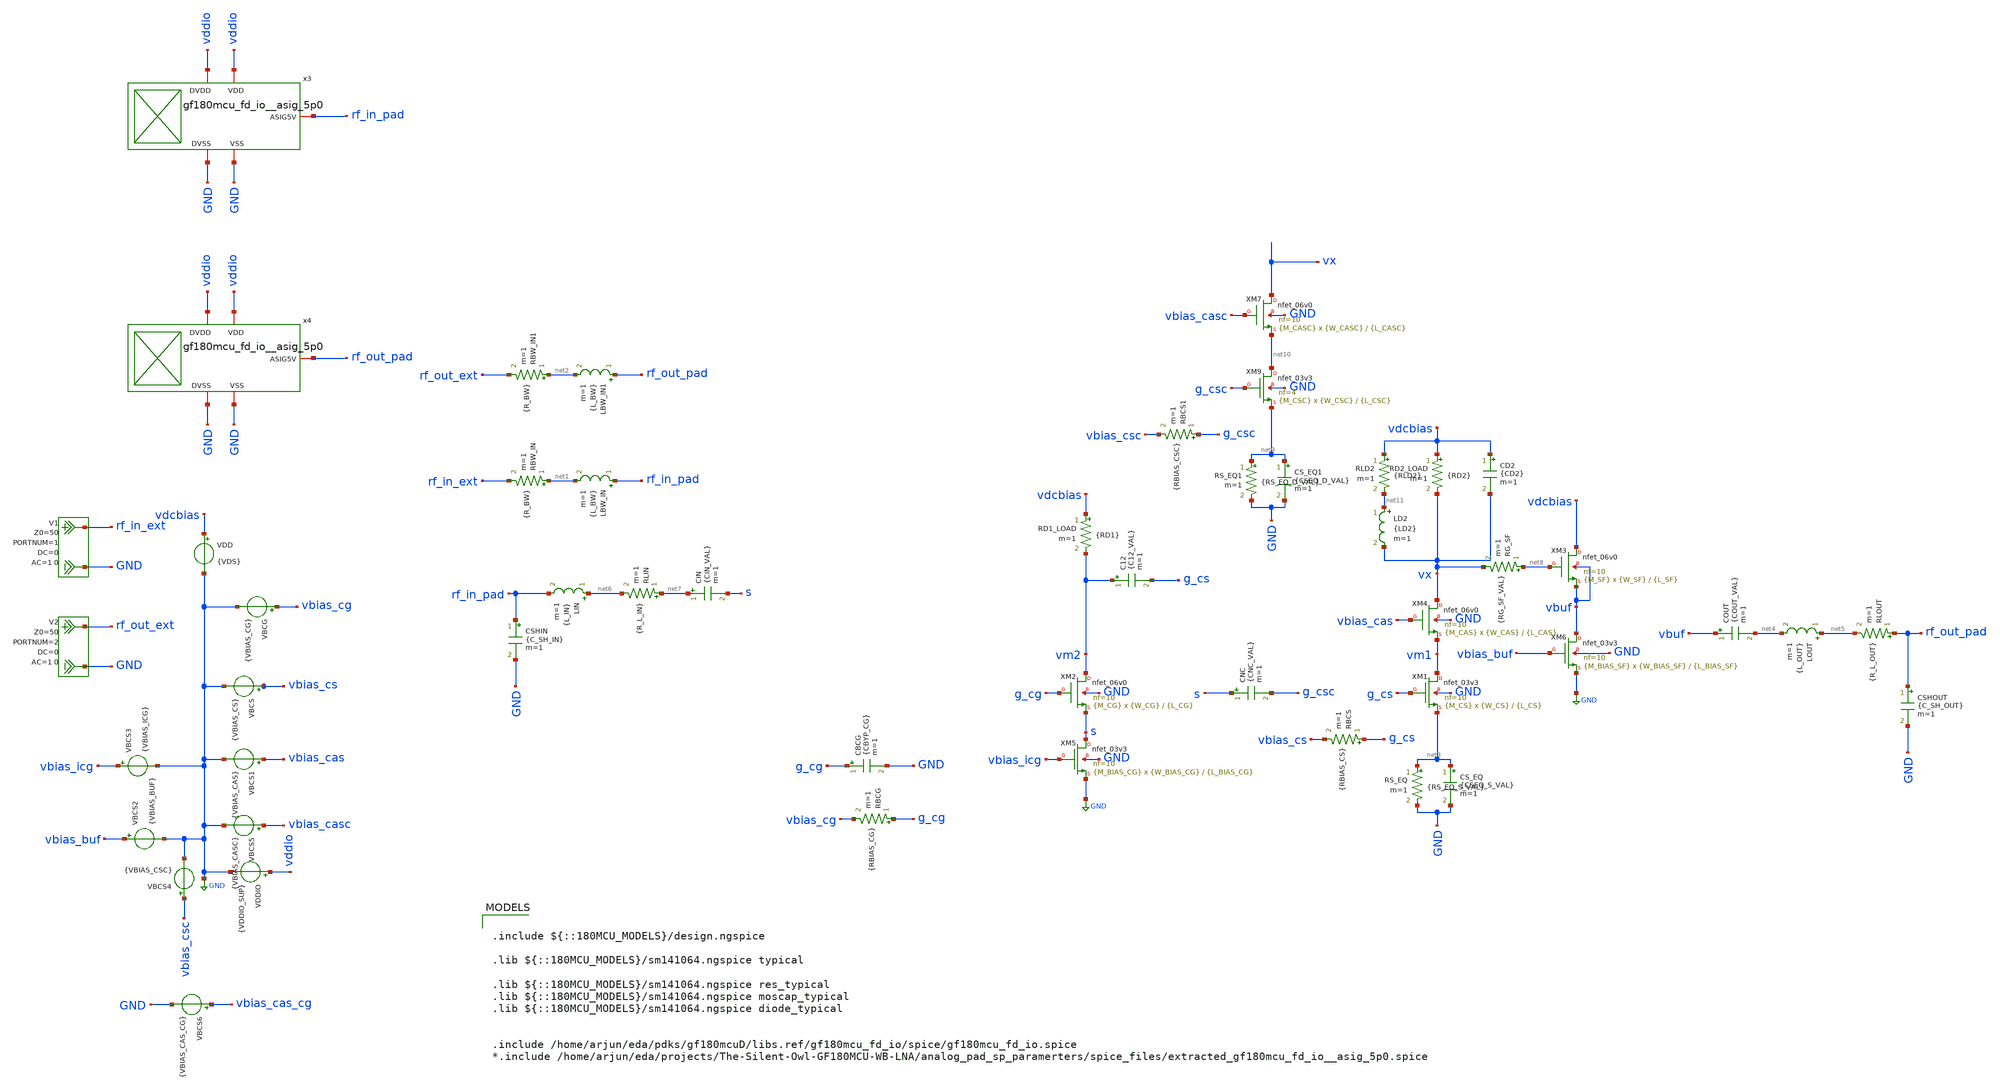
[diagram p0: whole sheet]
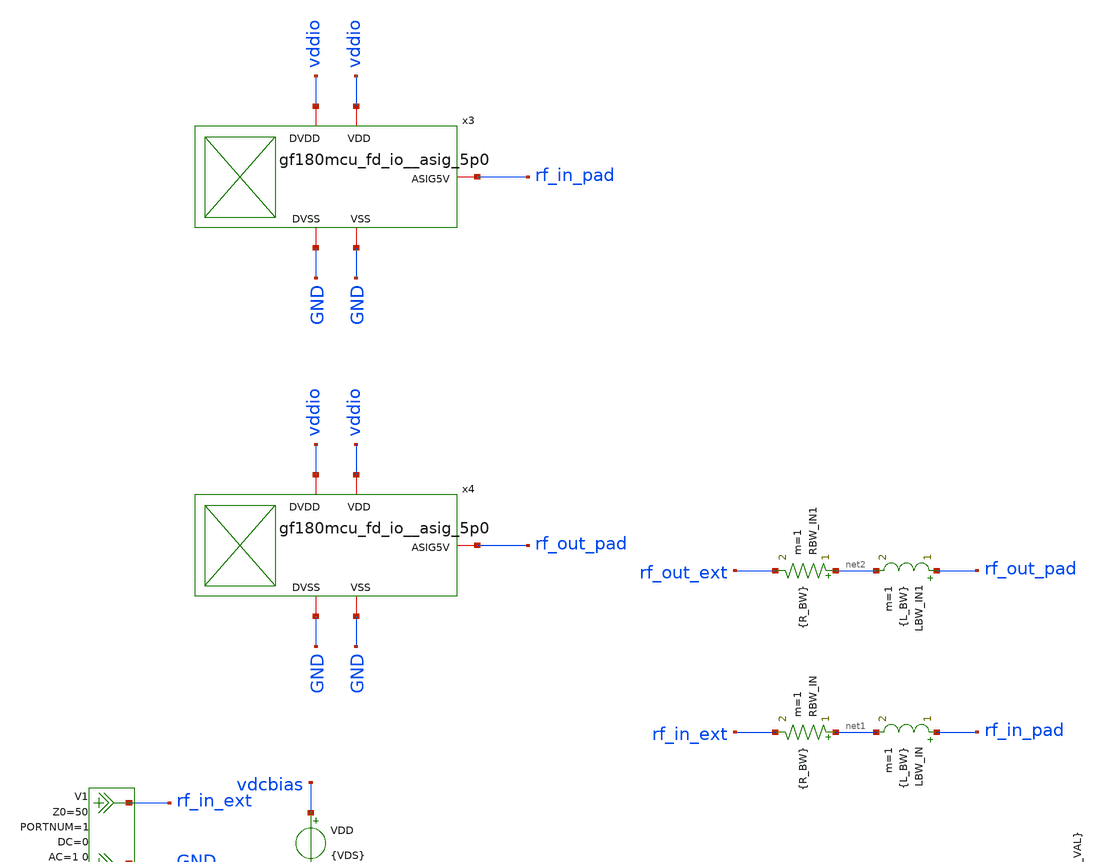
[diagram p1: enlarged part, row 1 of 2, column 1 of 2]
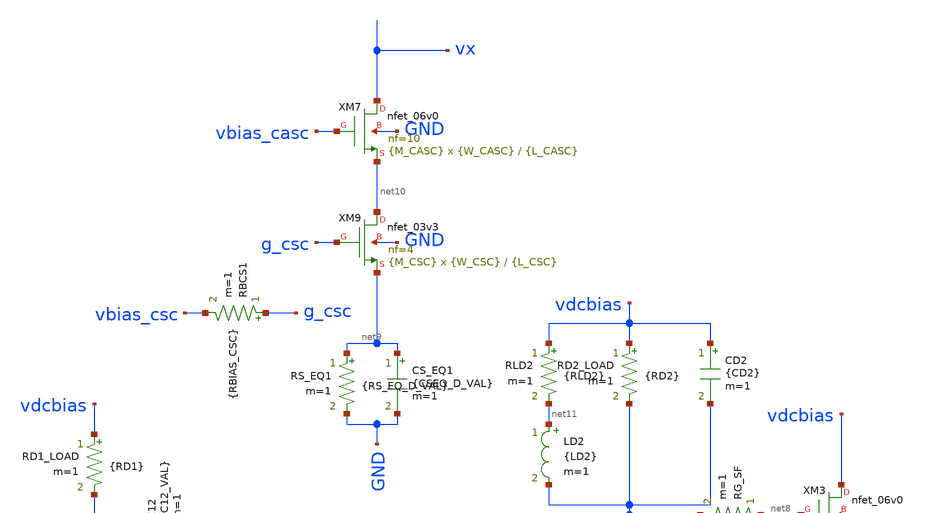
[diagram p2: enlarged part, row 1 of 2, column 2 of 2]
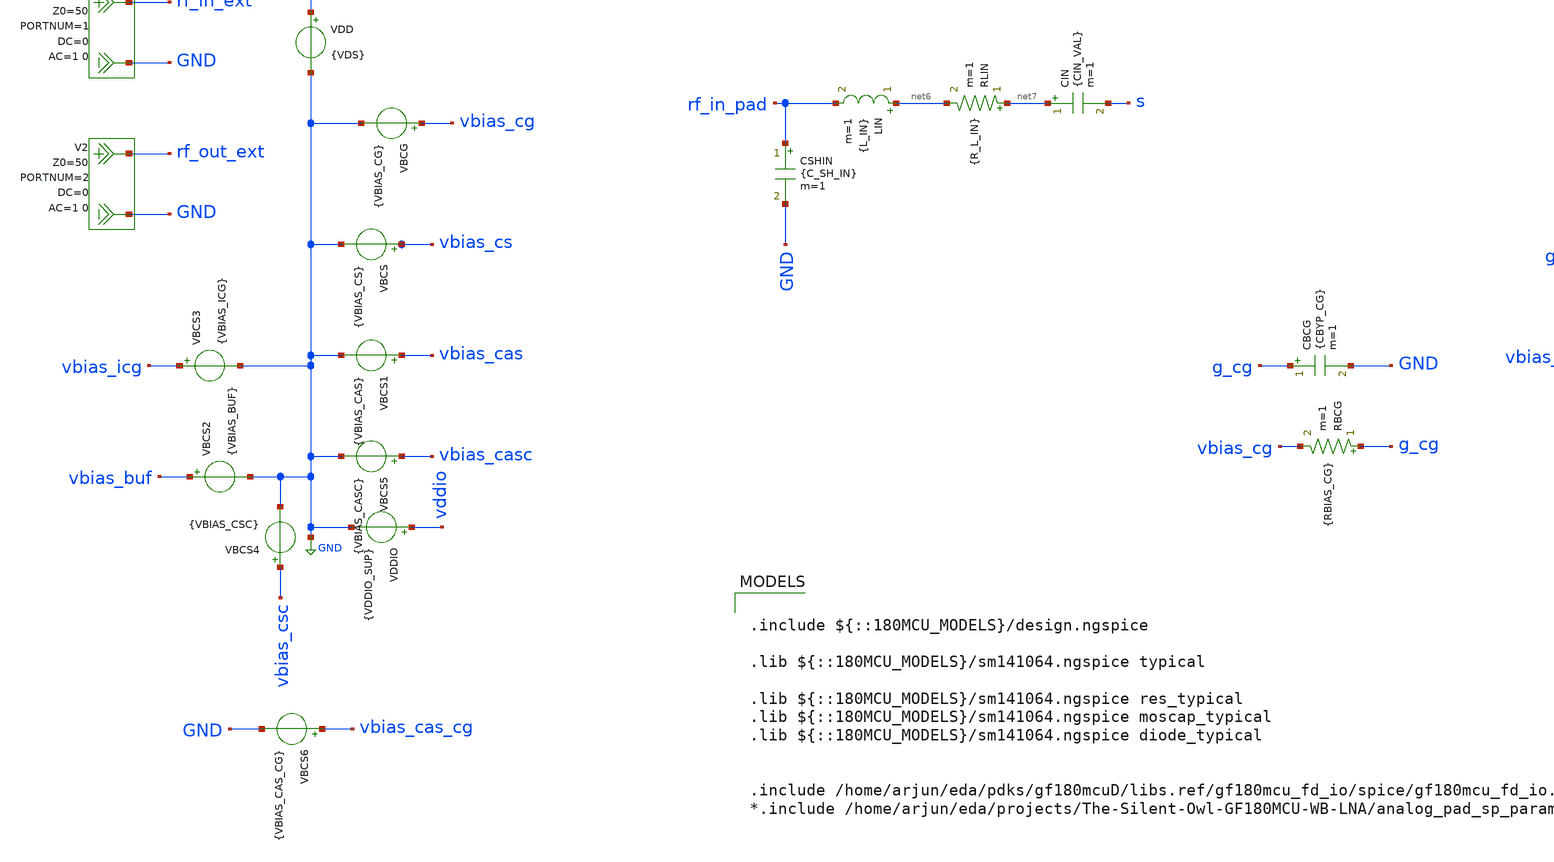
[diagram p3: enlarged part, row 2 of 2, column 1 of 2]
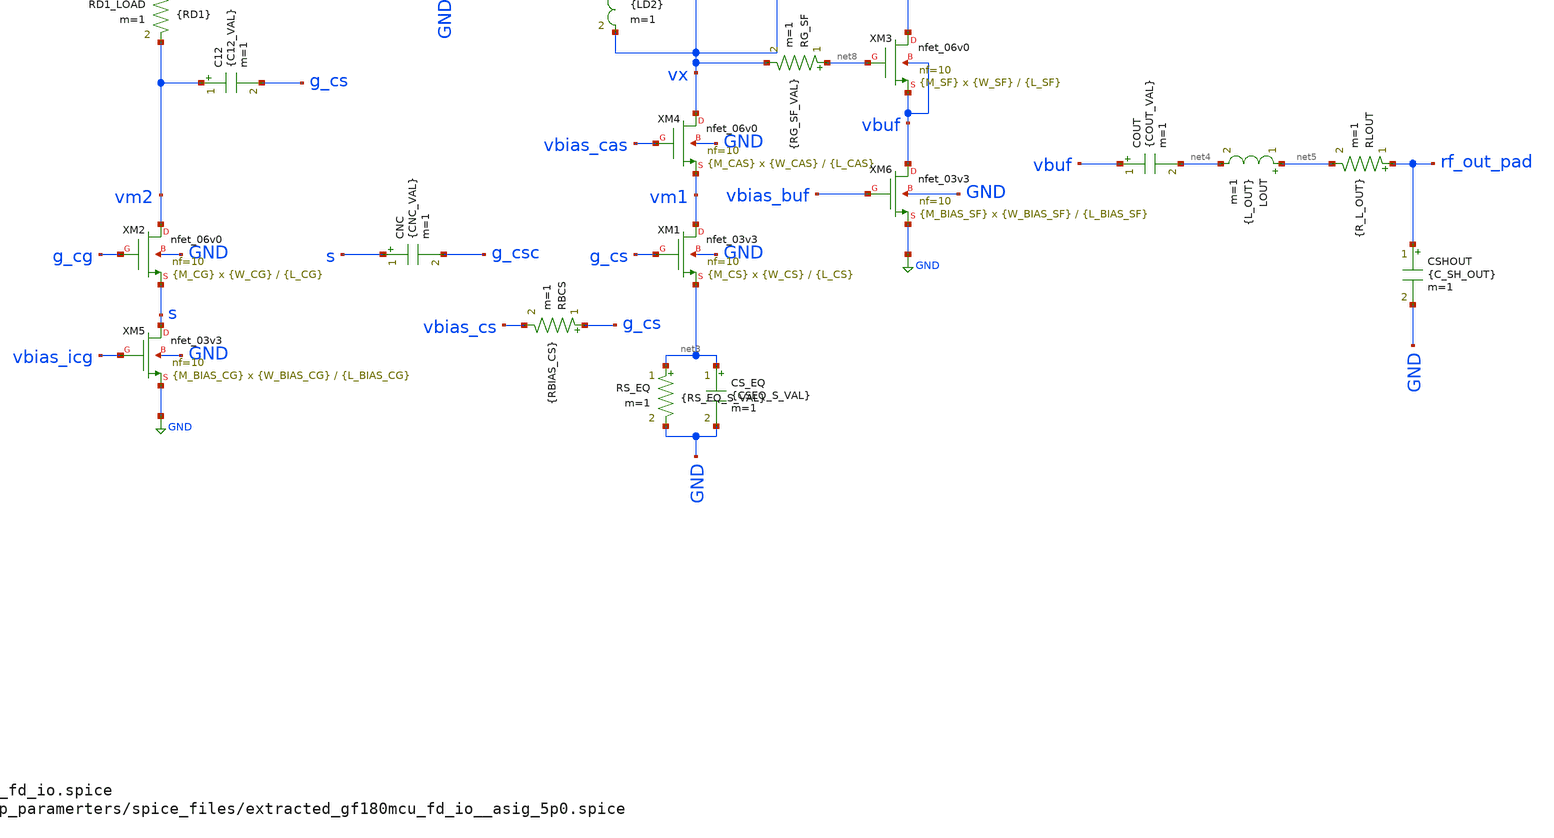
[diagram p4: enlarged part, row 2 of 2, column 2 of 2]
** sch_path: NFmin_Simulation/simulations/lna_core_06V_cgcs_sweep-1.sch
**.subckt lna_core_06V_cgcs_sweep-1
VBCG vbias_cg GND {VBIAS_CG}
VDD vdcbias GND {VDS}
C12 vm2 g_cs {C12_VAL} m=1
CIN net7 s {CIN_VAL} m=1
V1 rf_in_ext GND DC 0 AC 1 0 portnum 1 z0 50
V2 rf_out_ext GND DC 0 AC 1 0 portnum 2 z0 50
XM2 vm2 g_cg s GND nfet_06v0 L={L_CG} W={W_CG} nf=10 ad='int((nf+1)/2) * W/nf * 0.18u' as='int((nf+2)/2) * W/nf * 0.18u'
+ pd='2*int((nf+1)/2) * (W/nf + 0.18u)' ps='2*int((nf+2)/2) * (W/nf + 0.18u)' nrd='0.18u / W' nrs='0.18u / W'
+ sa=0 sb=0 sd=0 m={M_CG}
RBCG g_cg vbias_cg {RBIAS_CG} m=1
CBCG g_cg GND {CBYP_CG} m=1
LBW_IN rf_in_pad net1 {L_BW} m=1
RBW_IN net1 rf_in_ext {R_BW} m=1
VDDIO vddio GND {VDDIO_SUP}
LBW_IN1 rf_out_pad net2 {L_BW} m=1
RBW_IN1 net2 rf_out_ext {R_BW} m=1
VBCS vbias_cs GND {VBIAS_CS}
RD1_LOAD vdcbias vm2 {RD1} m=1
RBCS g_cs vbias_cs {RBIAS_CS} m=1
RD2_LOAD vdcbias vx {RD2} m=1
XM3 vdcbias net8 vbuf vbuf nfet_06v0 L={L_SF} W={W_SF} nf=10 ad='int((nf+1)/2) * W/nf * 0.18u' as='int((nf+2)/2) * W/nf * 0.18u'
+ pd='2*int((nf+1)/2) * (W/nf + 0.18u)' ps='2*int((nf+2)/2) * (W/nf + 0.18u)' nrd='0.18u / W' nrs='0.18u / W'
+ sa=0 sb=0 sd=0 m={M_SF}
COUT vbuf net4 {COUT_VAL} m=1
LOUT net5 net4 {L_OUT} m=1
RLOUT rf_out_pad net5 {R_L_OUT} m=1
CSHOUT rf_out_pad GND {C_SH_OUT} m=1
CSHIN rf_in_pad GND {C_SH_IN} m=1
LIN net6 rf_in_pad {L_IN} m=1
RLIN net7 net6 {R_L_IN} m=1
XM4 vx vbias_cas vm1 GND nfet_06v0 L={L_CAS} W={W_CAS} nf=10 ad='int((nf+1)/2) * W/nf * 0.18u' as='int((nf+2)/2) * W/nf * 0.18u'
+ pd='2*int((nf+1)/2) * (W/nf + 0.18u)' ps='2*int((nf+2)/2) * (W/nf + 0.18u)' nrd='0.18u / W' nrs='0.18u / W'
+ sa=0 sb=0 sd=0 m={M_CAS}
VBCS1 vbias_cas GND {VBIAS_CAS}
VBCS2 vbias_buf GND {VBIAS_BUF}
VBCS3 vbias_icg GND {VBIAS_ICG}
XM5 s vbias_icg GND GND nfet_03v3 L={L_BIAS_CG} W={W_BIAS_CG} nf=10 ad='int((nf+1)/2) * W/nf * 0.18u'
+ as='int((nf+2)/2) * W/nf * 0.18u' pd='2*int((nf+1)/2) * (W/nf + 0.18u)' ps='2*int((nf+2)/2) * (W/nf + 0.18u)'
+ nrd='0.18u / W' nrs='0.18u / W' sa=0 sb=0 sd=0 m={M_BIAS_CG}
XM6 vbuf vbias_buf GND GND nfet_03v3 L={L_BIAS_SF} W={W_BIAS_SF} nf=10 ad='int((nf+1)/2) * W/nf * 0.18u'
+ as='int((nf+2)/2) * W/nf * 0.18u' pd='2*int((nf+1)/2) * (W/nf + 0.18u)' ps='2*int((nf+2)/2) * (W/nf + 0.18u)'
+ nrd='0.18u / W' nrs='0.18u / W' sa=0 sb=0 sd=0 m={M_BIAS_SF}
RS_EQ net3 GND {RS_EQ_S_VAL} m=1
CS_EQ net3 GND {CSEQ_S_VAL} m=1
XM1 vm1 g_cs net3 GND nfet_03v3 L={L_CS} W={W_CS} nf=10 ad='int((nf+1)/2) * W/nf * 0.18u' as='int((nf+2)/2) * W/nf * 0.18u'
+ pd='2*int((nf+1)/2) * (W/nf + 0.18u)' ps='2*int((nf+2)/2) * (W/nf + 0.18u)' nrd='0.18u / W' nrs='0.18u / W'
+ sa=0 sb=0 sd=0 m={M_CS}
RG_SF net8 vx {RG_SF_VAL} m=1
x3 rf_in_pad vddio GND vddio GND gf180mcu_fd_io__asig_5p0
x4 rf_out_pad vddio GND vddio GND gf180mcu_fd_io__asig_5p0
RBCS1 g_csc vbias_csc {RBIAS_CSC} m=1
XM7 vx vbias_casc net10 GND nfet_06v0 L={L_CASC} W={W_CASC} nf=10 ad='int((nf+1)/2) * W/nf * 0.18u' as='int((nf+2)/2) * W/nf * 0.18u'
+ pd='2*int((nf+1)/2) * (W/nf + 0.18u)' ps='2*int((nf+2)/2) * (W/nf + 0.18u)' nrd='0.18u / W' nrs='0.18u / W'
+ sa=0 sb=0 sd=0 m={M_CASC}
RS_EQ1 net9 GND {RS_EQ_D_VAL} m=1
CS_EQ1 net9 GND {CSEQ_D_VAL} m=1
XM9 net10 g_csc net9 GND nfet_03v3 L={L_CSC} W={W_CSC} nf=4 ad='int((nf+1)/2) * W/nf * 0.18u' as='int((nf+2)/2) * W/nf * 0.18u'
+ pd='2*int((nf+1)/2) * (W/nf + 0.18u)' ps='2*int((nf+2)/2) * (W/nf + 0.18u)' nrd='0.18u / W' nrs='0.18u / W'
+ sa=0 sb=0 sd=0 m={M_CSC}
VBCS4 vbias_csc GND {VBIAS_CSC}
VBCS5 vbias_casc GND {VBIAS_CASC}
CNC s g_csc {CNC_VAL} m=1
VBCS6 vbias_cas_cg GND {VBIAS_CAS_CG}
LD2 net11 vx {LD2} m=1
CD2 vdcbias vx {CD2} m=1
RLD2 vdcbias net11 {RLD2} m=1
**** begin user architecture code

.include ${::180MCU_MODELS}/design.ngspice

.lib ${::180MCU_MODELS}/sm141064.ngspice typical

.lib ${::180MCU_MODELS}/sm141064.ngspice res_typical
.lib ${::180MCU_MODELS}/sm141064.ngspice moscap_typical
.lib ${::180MCU_MODELS}/sm141064.ngspice diode_typical


.include /home/arjun/eda/pdks/gf180mcuD/libs.ref/gf180mcu_fd_io/spice/gf180mcu_fd_io.spice
*.include /home/arjun/eda/projects/The-Silent-Owl-GF180MCU-WB-LNA/analog_pad_sp_paramerters/spice_files/extracted_gf180mcu_fd_io__asig_5p0.spice



* =============================================================================
* BEST OPTIMIZED PARAMETER SET
* =============================================================================
.param RLD2=7
* Currently unused unless a corresponding cascode-CG transistor is instantiated
.param VBIAS_CAS_CG=3.30
.param L_CAS_CG=0.60u
.param W_CAS_CG=80u
.param M_CAS_CG=4

* -----------------------------------------------------------------------------
* Supply / package
* -----------------------------------------------------------------------------
.param VDS=5.0
.param VDDIO_SUP=5.0

.param L_BW=2n
.param R_BW=0.2

* -----------------------------------------------------------------------------
* Source equalization networks
* -----------------------------------------------------------------------------

* XM9 cancellation-branch source equalizer
.param RS_EQ_D_VAL=0.25
.param CSEQ_D_VAL=4.7p

* XM1 main-path source equalizer
.param RS_EQ_S_VAL=0.10
.param CSEQ_S_VAL=220f

* Redundant aliases retained for compatibility
.param RS_EQ=0.10
.param CSEQ_VAL=220f

* -----------------------------------------------------------------------------
* Input network
*
* Package inductance       = 2.0 nH
* Intentional inductance   = 3.5 nH
* Total nominal inductance = 5.5 nH, excluding pad/interconnect parasitics
* -----------------------------------------------------------------------------
.param L_IN=3.5n
.param R_L_IN=2.26

.param CIN_VAL=8.2p
.param C_SH_IN=330f

* -----------------------------------------------------------------------------
* XM2 common-gate input stage
* -----------------------------------------------------------------------------
.param VBIAS_CG=2.10

.param W_CG=40u
.param M_CG=10
.param L_CG=0.60u

.param RD1=950

.param RBIAS_CG=50k
.param CBYP_CG=20p

* -----------------------------------------------------------------------------
* XM1 common-source / XM4 cascode main stage
* -----------------------------------------------------------------------------
.param C12_VAL=8.2p

.param VBIAS_CS=1.25

.param W_CS=20u
.param M_CS=8
.param L_CS=0.28u

.param RBIAS_CS=50k

.param VBIAS_CAS=3.60

.param W_CAS=35u
.param M_CAS=4
.param L_CAS=0.60u

.param RD2=1.2k

* -----------------------------------------------------------------------------
* XM3 body-tied source follower
* -----------------------------------------------------------------------------
.param W_SF=25u
.param M_SF=8
.param L_SF=0.60u

.param RG_SF_VAL=0.10

* -----------------------------------------------------------------------------
* Output network
*
* Package inductance       = 2.0 nH
* Intentional inductance   = 1.2 nH
* Total nominal inductance = 3.2 nH, excluding pad/interconnect parasitics
* -----------------------------------------------------------------------------
.param COUT_VAL=4.7p

.param L_OUT=1.2n
.param R_L_OUT=1.5

.param C_SH_OUT=470f

* -----------------------------------------------------------------------------
* XM5 common-gate current sink
* -----------------------------------------------------------------------------
.param VBIAS_ICG=1.80

.param L_BIAS_CG=0.50u
.param W_BIAS_CG=15u
.param M_BIAS_CG=1

* -----------------------------------------------------------------------------
* XM6 source-follower current sink
* -----------------------------------------------------------------------------
.param VBIAS_BUF=2.50

.param L_BIAS_SF=0.50u
.param W_BIAS_SF=25u
.param M_BIAS_SF=5

* -----------------------------------------------------------------------------
* XM9 source-sensing common-source cancellation branch
* -----------------------------------------------------------------------------
.param RBIAS_CSC=50k

.param VBIAS_CSC=0.90

.param L_CSC=0.28u
.param W_CSC=40u
.param M_CSC=6
.param NF_CSC=4

* -----------------------------------------------------------------------------
* XM7 cancellation-branch cascode
* -----------------------------------------------------------------------------
.param VBIAS_CASC=3.40

.param L_CASC=0.60u
.param W_CASC=35u
.param M_CASC=1

* -----------------------------------------------------------------------------
* Noise-cancellation coupling capacitor
* -----------------------------------------------------------------------------
.param CNC_VAL=8.2p

* -----------------------------------------------------------------------------
* Drain shunt-peaking network
* -----------------------------------------------------------------------------
.param LD2=4.7n
.param CD2=680f
.param R_LD2=7





.control

set noaskquit
set wr_singlescale
set wr_vecnames
set numdgt=10

let target_gain_bw=10.0

echo ============================================================ > lna_core_06V_cgcs_report.txt
echo GF180MCU_LNA_CORE_06V_CGCS_DETAILED_REPORT >> lna_core_06V_cgcs_report.txt
echo TARGET_FREQUENCY_HZ 2.400e9 >> lna_core_06V_cgcs_report.txt
echo TARGET_BAND_HZ 2.300e9 2.500e9 >> lna_core_06V_cgcs_report.txt
echo GAIN_BANDWIDTH_THRESHOLD_DB 10.0 >> lna_core_06V_cgcs_report.txt
echo PORT_REFERENCE_OHM 50 >> lna_core_06V_cgcs_report.txt
echo ============================================================ >> lna_core_06V_cgcs_report.txt

* =============================================================================
* DC OPERATING POINT
* =============================================================================

op

let pdcop=1e3*(abs(i(VDD))*v(vdcbias)+abs(i(VDDIO))*v(vddio))
let icoreop=abs(i(VDD))
let iioop=abs(i(VDDIO))

let vsop=v(s)
let vdop=v(vm2)
let vnet3op=v(net3)
let vnet8op=v(net8)
let vbufop=v(vbuf)
let vgcsop=v(g_cs)
let vgcgop=v(g_cg)

let id1op=abs(@m.xm1.m0[id])
let gm1op=@m.xm1.m0[gm]
let gmb1op=@m.xm1.m0[gmbs]
let gds1op=@m.xm1.m0[gds]
let vgs1op=@m.xm1.m0[vgs]
let vds1op=@m.xm1.m0[vds]
let vbs1op=@m.xm1.m0[vbs]
let vth1op=@m.xm1.m0[vth]
let vov1op=vgs1op-vth1op
let vdsat1op=abs(@m.xm1.m0[vdsat])
let sat1op=vds1op-vdsat1op
let gmid1op=gm1op/(id1op+1e-30)
let ro1op=1/(gds1op+1e-30)

let id2op=abs(@m.xm2.m0[id])
let gm2op=@m.xm2.m0[gm]
let gmb2op=@m.xm2.m0[gmbs]
let gds2op=@m.xm2.m0[gds]
let vgs2op=@m.xm2.m0[vgs]
let vds2op=@m.xm2.m0[vds]
let vbs2op=@m.xm2.m0[vbs]
let vth2op=@m.xm2.m0[vth]
let vov2op=vgs2op-vth2op
let vdsat2op=abs(@m.xm2.m0[vdsat])
let sat2op=vds2op-vdsat2op
let gmid2op=gm2op/(id2op+1e-30)
let ro2op=1/(gds2op+1e-30)

let id3op=abs(@m.xm3.m0[id])
let gm3op=@m.xm3.m0[gm]
let gmb3op=@m.xm3.m0[gmbs]
let gds3op=@m.xm3.m0[gds]
let vgs3op=@m.xm3.m0[vgs]
let vds3op=@m.xm3.m0[vds]
let vbs3op=@m.xm3.m0[vbs]
let vth3op=@m.xm3.m0[vth]
let vov3op=vgs3op-vth3op
let vdsat3op=abs(@m.xm3.m0[vdsat])
let sat3op=vds3op-vdsat3op
let gmid3op=gm3op/(id3op+1e-30)
let ro3op=1/(gds3op+1e-30)

let id4op=abs(@m.xm4.m0[id])
let gm4op=@m.xm4.m0[gm]
let gmb4op=@m.xm4.m0[gmbs]
let gds4op=@m.xm4.m0[gds]
let vgs4op=@m.xm4.m0[vgs]
let vds4op=@m.xm4.m0[vds]
let vbs4op=@m.xm4.m0[vbs]
let vth4op=@m.xm4.m0[vth]
let vov4op=vgs4op-vth4op
let vdsat4op=abs(@m.xm4.m0[vdsat])
let sat4op=vds4op-vdsat4op
let gmid4op=gm4op/(id4op+1e-30)
let ro4op=1/(gds4op+1e-30)

let id5op=abs(@m.xm5.m0[id])
let gm5op=@m.xm5.m0[gm]
let gmb5op=@m.xm5.m0[gmbs]
let gds5op=@m.xm5.m0[gds]
let vgs5op=@m.xm5.m0[vgs]
let vds5op=@m.xm5.m0[vds]
let vbs5op=@m.xm5.m0[vbs]
let vth5op=@m.xm5.m0[vth]
let vov5op=vgs5op-vth5op
let vdsat5op=abs(@m.xm5.m0[vdsat])
let sat5op=vds5op-vdsat5op
let gmid5op=gm5op/(id5op+1e-30)
let ro5op=1/(gds5op+1e-30)

let id6op=abs(@m.xm6.m0[id])
let gm6op=@m.xm6.m0[gm]
let gmb6op=@m.xm6.m0[gmbs]
let gds6op=@m.xm6.m0[gds]
let vgs6op=@m.xm6.m0[vgs]
let vds6op=@m.xm6.m0[vds]
let vbs6op=@m.xm6.m0[vbs]
let vth6op=@m.xm6.m0[vth]
let vov6op=vgs6op-vth6op
let vdsat6op=abs(@m.xm6.m0[vdsat])
let sat6op=vds6op-vdsat6op
let gmid6op=gm6op/(id6op+1e-30)
let ro6op=1/(gds6op+1e-30)

let id7op=abs(@m.xm7.m0[id])
let gm7op=@m.xm7.m0[gm]
let gmb7op=@m.xm7.m0[gmbs]
let gds7op=@m.xm7.m0[gds]
let vgs7op=@m.xm7.m0[vgs]
let vds7op=@m.xm7.m0[vds]
let vbs7op=@m.xm7.m0[vbs]
let vth7op=@m.xm7.m0[vth]
let vov7op=vgs7op-vth7op
let vdsat7op=abs(@m.xm7.m0[vdsat])
let sat7op=vds7op-vdsat7op
let gmid7op=gm7op/(id7op+1e-30)
let ro7op=1/(gds7op+1e-30)

let id9op=abs(@m.xm9.m0[id])
let gm9op=@m.xm9.m0[gm]
let gmb9op=@m.xm9.m0[gmbs]
let gds9op=@m.xm9.m0[gds]
let vgs9op=@m.xm9.m0[vgs]
let vds9op=@m.xm9.m0[vds]
let vbs9op=@m.xm9.m0[vbs]
let vth9op=@m.xm9.m0[vth]
let vov9op=vgs9op-vth9op
let vdsat9op=abs(@m.xm9.m0[vdsat])
let sat9op=vds9op-vdsat9op
let gmid9op=gm9op/(id9op+1e-30)
let ro9op=1/(gds9op+1e-30)

let vnet9op=vnet3op+vds1op
let vnet9check=vnet8op-vds4op
let vnet9diff=vnet9op-vnet9check
let vnet10op=vsop+vds2op
let vnet10check=vdop-vds7op
let vnet10diff=vnet10op-vnet10check

set op_pdc=$&pdcop
set op_icore=$&icoreop
set op_iio=$&iioop
set op_vs=$&vsop
set op_vnet10=$&vnet10op
set op_vnet10check=$&vnet10check
set op_vnet10diff=$&vnet10diff
set op_vd=$&vdop
set op_vnet3=$&vnet3op
set op_vnet9=$&vnet9op
set op_vnet9check=$&vnet9check
set op_vnet9diff=$&vnet9diff
set op_vnet8=$&vnet8op
set op_vbuf=$&vbufop
set op_vgcs=$&vgcsop
set op_vgcg=$&vgcgop

set op_id1=$&id1op
set op_gm1=$&gm1op
set op_gmb1=$&gmb1op
set op_gds1=$&gds1op
set op_vgs1=$&vgs1op
set op_vds1=$&vds1op
set op_vbs1=$&vbs1op
set op_vth1=$&vth1op
set op_vov1=$&vov1op
set op_vdsat1=$&vdsat1op
set op_sat1=$&sat1op
set op_gmid1=$&gmid1op
set op_ro1=$&ro1op

set op_id2=$&id2op
set op_gm2=$&gm2op
set op_gmb2=$&gmb2op
set op_gds2=$&gds2op
set op_vgs2=$&vgs2op
set op_vds2=$&vds2op
set op_vbs2=$&vbs2op
set op_vth2=$&vth2op
set op_vov2=$&vov2op
set op_vdsat2=$&vdsat2op
set op_sat2=$&sat2op
set op_gmid2=$&gmid2op
set op_ro2=$&ro2op

set op_id3=$&id3op
set op_gm3=$&gm3op
set op_gmb3=$&gmb3op
set op_gds3=$&gds3op
set op_vgs3=$&vgs3op
set op_vds3=$&vds3op
set op_vbs3=$&vbs3op
set op_vth3=$&vth3op
set op_vov3=$&vov3op
set op_vdsat3=$&vdsat3op
set op_sat3=$&sat3op
set op_gmid3=$&gmid3op
set op_ro3=$&ro3op

set op_id4=$&id4op
set op_gm4=$&gm4op
set op_gmb4=$&gmb4op
set op_gds4=$&gds4op
set op_vgs4=$&vgs4op
set op_vds4=$&vds4op
set op_vbs4=$&vbs4op
set op_vth4=$&vth4op
set op_vov4=$&vov4op
set op_vdsat4=$&vdsat4op
set op_sat4=$&sat4op
set op_gmid4=$&gmid4op
set op_ro4=$&ro4op

set op_id5=$&id5op
set op_gm5=$&gm5op
set op_gmb5=$&gmb5op
set op_gds5=$&gds5op
set op_vgs5=$&vgs5op
set op_vds5=$&vds5op
set op_vbs5=$&vbs5op
set op_vth5=$&vth5op
set op_vov5=$&vov5op
set op_vdsat5=$&vdsat5op
set op_sat5=$&sat5op
set op_gmid5=$&gmid5op
set op_ro5=$&ro5op

set op_id6=$&id6op
set op_gm6=$&gm6op
set op_gmb6=$&gmb6op
set op_gds6=$&gds6op
set op_vgs6=$&vgs6op
set op_vds6=$&vds6op
set op_vbs6=$&vbs6op
set op_vth6=$&vth6op
set op_vov6=$&vov6op
set op_vdsat6=$&vdsat6op
set op_sat6=$&sat6op
set op_gmid6=$&gmid6op
set op_ro6=$&ro6op

set op_id7=$&id7op
set op_gm7=$&gm7op
set op_gmb7=$&gmb7op
set op_gds7=$&gds7op
set op_vgs7=$&vgs7op
set op_vds7=$&vds7op
set op_vbs7=$&vbs7op
set op_vth7=$&vth7op
set op_vov7=$&vov7op
set op_vdsat7=$&vdsat7op
set op_sat7=$&sat7op
set op_gmid7=$&gmid7op
set op_ro7=$&ro7op

set op_id9=$&id9op
set op_gm9=$&gm9op
set op_gmb9=$&gmb9op
set op_gds9=$&gds9op
set op_vgs9=$&vgs9op
set op_vds9=$&vds9op
set op_vbs9=$&vbs9op
set op_vth9=$&vth9op
set op_vov9=$&vov9op
set op_vdsat9=$&vdsat9op
set op_sat9=$&sat9op
set op_gmid9=$&gmid9op
set op_ro9=$&ro9op

echo ============================================================ >> lna_core_06V_cgcs_report.txt
echo DC_SUPPLY_AND_NODE_VOLTAGES >> lna_core_06V_cgcs_report.txt
echo PDC_mW $op_pdc ICORE_A $op_icore IIO_A $op_iio >> lna_core_06V_cgcs_report.txt
echo NODES_V S $op_vs NET10_DERIVED $op_vnet10 VM2 $op_vd NET3 $op_vnet3 NET9_DERIVED $op_vnet9 NET8
+ $op_vnet8 VBUF $op_vbuf G_CS $op_vgcs G_CG $op_vgcg >> lna_core_06V_cgcs_report.txt
echo HIDDEN_NODE_CHECKS NET10_FROM_XM2 $op_vnet10 NET10_FROM_XM7 $op_vnet10check DIFFERENCE
+ $op_vnet10diff NET9_FROM_XM1 $op_vnet9 NET9_FROM_XM4 $op_vnet9check DIFFERENCE $op_vnet9diff >>
+ lna_core_06V_cgcs_report.txt
echo ============================================================ >> lna_core_06V_cgcs_report.txt
echo TRANSISTOR_OPERATING_POINTS >> lna_core_06V_cgcs_report.txt
echo FIELDS ID_A GM_S GMBS_S GDS_S VGS_V VDS_V VBS_V VTH_V VOV_V VDSAT_V SAT_MARGIN_V
+ GM_OVER_ID_1_PER_V RO_OHM >> lna_core_06V_cgcs_report.txt
echo XM1_CS ID $op_id1 GM $op_gm1 GMBS $op_gmb1 GDS $op_gds1 VGS $op_vgs1 VDS $op_vds1 VBS $op_vbs1
+ VTH $op_vth1 VOV $op_vov1 VDSAT $op_vdsat1 SAT_MARGIN $op_sat1 GMID $op_gmid1 RO $op_ro1 >>
+ lna_core_06V_cgcs_report.txt
echo XM2_CG ID $op_id2 GM $op_gm2 GMBS $op_gmb2 GDS $op_gds2 VGS $op_vgs2 VDS $op_vds2 VBS $op_vbs2
+ VTH $op_vth2 VOV $op_vov2 VDSAT $op_vdsat2 SAT_MARGIN $op_sat2 GMID $op_gmid2 RO $op_ro2 >>
+ lna_core_06V_cgcs_report.txt
echo XM3_SOURCE_FOLLOWER ID $op_id3 GM $op_gm3 GMBS $op_gmb3 GDS $op_gds3 VGS $op_vgs3 VDS $op_vds3
+ VBS $op_vbs3 VTH $op_vth3 VOV $op_vov3 VDSAT $op_vdsat3 SAT_MARGIN $op_sat3 GMID $op_gmid3 RO $op_ro3
+ >> lna_core_06V_cgcs_report.txt
echo XM4_CS_CASCODE ID $op_id4 GM $op_gm4 GMBS $op_gmb4 GDS $op_gds4 VGS $op_vgs4 VDS $op_vds4 VBS
+ $op_vbs4 VTH $op_vth4 VOV $op_vov4 VDSAT $op_vdsat4 SAT_MARGIN $op_sat4 GMID $op_gmid4 RO $op_ro4 >>
+ lna_core_06V_cgcs_report.txt
echo XM5_CG_CURRENT_SINK ID $op_id5 GM $op_gm5 GMBS $op_gmb5 GDS $op_gds5 VGS $op_vgs5 VDS $op_vds5
+ VBS $op_vbs5 VTH $op_vth5 VOV $op_vov5 VDSAT $op_vdsat5 SAT_MARGIN $op_sat5 GMID $op_gmid5 RO $op_ro5
+ >> lna_core_06V_cgcs_report.txt
echo XM6_BUFFER_CURRENT_SINK ID $op_id6 GM $op_gm6 GMBS $op_gmb6 GDS $op_gds6 VGS $op_vgs6 VDS
+ $op_vds6 VBS $op_vbs6 VTH $op_vth6 VOV $op_vov6 VDSAT $op_vdsat6 SAT_MARGIN $op_sat6 GMID $op_gmid6 RO
+ $op_ro6 >> lna_core_06V_cgcs_report.txt
echo XM7_CG_CASCODE ID $op_id7 GM $op_gm7 GMBS $op_gmb7 GDS $op_gds7 VGS $op_vgs7 VDS $op_vds7 VBS
+ $op_vbs7 VTH $op_vth7 VOV $op_vov7 VDSAT $op_vdsat7 SAT_MARGIN $op_sat7 GMID $op_gmid7 RO $op_ro7 >>
+ lna_core_06V_cgcs_report.txt
echo XM9_CANCELLATION_CS ID $op_id9 GM $op_gm9 GMBS $op_gmb9 GDS $op_gds9 VGS $op_vgs9 VDS $op_vds9
+ VBS $op_vbs9 VTH $op_vth9 VOV $op_vov9 VDSAT $op_vdsat9 SAT_MARGIN $op_sat9 GMID $op_gmid9 RO $op_ro9
+ >> lna_core_06V_cgcs_report.txt

destroy $curplot

* =============================================================================
* SINGLE BROADBAND RF ANALYSIS
* One reset and one SP run are used for all 1 MHz to 7 GHz RF results.
* Target-band values are extracted from the same dataset.
* This avoids inconsistent port excitation state between repeated SP runs.
* 7000 points from 1 MHz to 7 GHz gives exactly 1 MHz spacing.
* =============================================================================

reset
sp lin 7000 1Meg 7Gig 1
set rfplot=$curplot

let fghz=frequency/1e9

let s11db=db(s_1_1)
let s21db=db(s_2_1)
let s12db=db(s_1_2)
let s22db=db(s_2_2)

let s11re=real(s_1_1)
let s11im=imag(s_1_1)
let s21re=real(s_2_1)
let s21im=imag(s_2_1)
let s12re=real(s_1_2)
let s12im=imag(s_1_2)
let s22re=real(s_2_2)
let s22im=imag(s_2_2)

let nfdb=real(NF)
let nfmin_db=real(NFmin)

let delta=s_1_1*s_2_2-s_1_2*s_2_1
let delta_mag=mag(delta)
let a11=mag(s_1_1)
let a12=mag(s_1_2)
let a21=mag(s_2_1)
let a22=mag(s_2_2)
let mu=(1-a11*a11)/(mag(s_2_2-delta*conj(s_1_1))+mag(s_1_2*s_2_1))
let mup=(1-a22*a22)/(mag(s_1_1-delta*conj(s_2_2))+mag(s_1_2*s_2_1))
let kval=(1-a11*a11-a22*a22+delta_mag*delta_mag)/(2*a12*a21)

let zin=50*(1+s_1_1)/(1-s_1_1)
let zout=50*(1+s_2_2)/(1-s_2_2)
let zin_re=real(zin)
let zin_im=imag(zin)
let zout_re=real(zout)
let zout_im=imag(zout)

let npts=length(frequency)

* Find indices nearest 2.300 GHz, 2.400 GHz and 2.500 GHz.
let ilo=0
let icenter=0
let ihi=0
let errlo=abs(frequency[0]-2.3e9)
let errcenter=abs(frequency[0]-2.4e9)
let errhi=abs(frequency[0]-2.5e9)
let ii=1
while ii < npts
let newerr=abs(frequency[ii]-2.3e9)
if newerr < errlo
let errlo=newerr
let ilo=ii
end
let newerr=abs(frequency[ii]-2.4e9)
if newerr < errcenter
let errcenter=newerr
let icenter=ii
end
let newerr=abs(frequency[ii]-2.5e9)
if newerr < errhi
let errhi=newerr
let ihi=ii
end
let ii=ii+1
end

* Values at the sample nearest 2.400 GHz.
let center_freq=frequency[icenter]
let s11c=s11db[icenter]
let s21c=s21db[icenter]
let s12c=s12db[icenter]
let s22c=s22db[icenter]
let s11rc=s11re[icenter]
let s11ic=s11im[icenter]
let s21rc=s21re[icenter]
let s21ic=s21im[icenter]
let s12rc=s12re[icenter]
let s12ic=s12im[icenter]
let s22rc=s22re[icenter]
let s22ic=s22im[icenter]
let nfc=nfdb[icenter]
let nfminc=nfmin_db[icenter]
let muc=mu[icenter]
let mupc=mup[icenter]
let kc=kval[icenter]
let dmc=delta_mag[icenter]
let zinrc=zin_re[icenter]
let zinic=zin_im[icenter]
let zoutrc=zout_re[icenter]
let zoutic=zout_im[icenter]

* Initialize target-band extrema.
let s11min=s11db[ilo]
let s11max=s11db[ilo]
let s21min=s21db[ilo]
let s21max=s21db[ilo]
let s12min=s12db[ilo]
let s12max=s12db[ilo]
let s22min=s22db[ilo]
let s22max=s22db[ilo]
let nfbandmin=nfdb[ilo]
let nfbandmax=nfdb[ilo]
let nfminbandmin=nfmin_db[ilo]
let nfminbandmax=nfmin_db[ilo]
let mumin=mu[ilo]
let mupmin=mup[ilo]
let kmin=kval[ilo]
let dmax=delta_mag[ilo]

let s11min_i=ilo
let s11max_i=ilo
let s21min_i=ilo
let s21max_i=ilo
let s12min_i=ilo
let s12max_i=ilo
let s22min_i=ilo
let s22max_i=ilo
let nfmin_i=ilo
let nfmax_i=ilo
let nfminpar_min_i=ilo
let nfminpar_max_i=ilo
let mumin_i=ilo
let mupmin_i=ilo
let kmin_i=ilo
let dmax_i=ilo

* Scan 2.300 GHz to 2.500 GHz.
let ii=ilo
while ii <= ihi
if s11db[ii] < s11min
let s11min=s11db[ii]
let s11min_i=ii
end
if s11db[ii] > s11max
let s11max=s11db[ii]
let s11max_i=ii
end
if s21db[ii] < s21min
let s21min=s21db[ii]
let s21min_i=ii
end
if s21db[ii] > s21max
let s21max=s21db[ii]
let s21max_i=ii
end
if s12db[ii] < s12min
let s12min=s12db[ii]
let s12min_i=ii
end
if s12db[ii] > s12max
let s12max=s12db[ii]
let s12max_i=ii
end
if s22db[ii] < s22min
let s22min=s22db[ii]
let s22min_i=ii
end
if s22db[ii] > s22max
let s22max=s22db[ii]
let s22max_i=ii
end
if nfdb[ii] < nfbandmin
let nfbandmin=nfdb[ii]
let nfmin_i=ii
end
if nfdb[ii] > nfbandmax
let nfbandmax=nfdb[ii]
let nfmax_i=ii
end
if nfmin_db[ii] < nfminbandmin
let nfminbandmin=nfmin_db[ii]
let nfminpar_min_i=ii
end
if nfmin_db[ii] > nfminbandmax
let nfminbandmax=nfmin_db[ii]
let nfminpar_max_i=ii
end
if mu[ii] < mumin
let mumin=mu[ii]
let mumin_i=ii
end
if mup[ii] < mupmin
let mupmin=mup[ii]
let mupmin_i=ii
end
if kval[ii] < kmin
let kmin=kval[ii]
let kmin_i=ii
end
if delta_mag[ii] > dmax
let dmax=delta_mag[ii]
let dmax_i=ii
end
let ii=ii+1
end

let gain_ripple=s21max-s21min

let s11min_f=frequency[s11min_i]
let s11max_f=frequency[s11max_i]
let s21min_f=frequency[s21min_i]
let s21max_f=frequency[s21max_i]
let s12min_f=frequency[s12min_i]
let s12max_f=frequency[s12max_i]
let s22min_f=frequency[s22min_i]
let s22max_f=frequency[s22max_i]
let nfmin_f=frequency[nfmin_i]
let nfmax_f=frequency[nfmax_i]
let nfminpar_min_f=frequency[nfminpar_min_i]
let nfminpar_max_f=frequency[nfminpar_max_i]
let mumin_f=frequency[mumin_i]
let mupmin_f=frequency[mupmin_i]
let kmin_f=frequency[kmin_i]
let dmax_f=frequency[dmax_i]

* Find the broadband S21 peak and its index.
let imax=0
let gainmax=s21db[0]
let ii=1
while ii < npts
if s21db[ii] > gainmax
let gainmax=s21db[ii]
let imax=ii
end
let ii=ii+1
end
let peakfreq=frequency[imax]

echo ============================================================ >> lna_core_06V_cgcs_report.txt
echo RF_AT_2P400_GHZ_FROM_SINGLE_BROADBAND_SWEEP >> lna_core_06V_cgcs_report.txt
echo ACTUAL_SAMPLE_HZ $&center_freq >> lna_core_06V_cgcs_report.txt
echo S11_DB $&s11c REAL $&s11rc IMAG $&s11ic >> lna_core_06V_cgcs_report.txt
echo S21_DB $&s21c REAL $&s21rc IMAG $&s21ic >> lna_core_06V_cgcs_report.txt
echo S12_DB $&s12c REAL $&s12rc IMAG $&s12ic >> lna_core_06V_cgcs_report.txt
echo S22_DB $&s22c REAL $&s22rc IMAG $&s22ic >> lna_core_06V_cgcs_report.txt
echo NF_DB $&nfc NFMIN_DB $&nfminc >> lna_core_06V_cgcs_report.txt
echo MU $&muc MUP $&mupc K $&kc DELTA_MAG $&dmc >> lna_core_06V_cgcs_report.txt
echo ZIN_OHM RE $&zinrc IM $&zinic >> lna_core_06V_cgcs_report.txt
echo ZOUT_OHM RE $&zoutrc IM $&zoutic >> lna_core_06V_cgcs_report.txt

echo ============================================================ >> lna_core_06V_cgcs_report.txt
echo RF_MIN_MAX_FROM_2P300_TO_2P500_GHZ >> lna_core_06V_cgcs_report.txt
echo S11_MIN_DB $&s11min AT_HZ $&s11min_f S11_MAX_DB $&s11max AT_HZ $&s11max_f >>
+ lna_core_06V_cgcs_report.txt
echo S21_MIN_DB $&s21min AT_HZ $&s21min_f S21_MAX_DB $&s21max AT_HZ $&s21max_f GAIN_RIPPLE_DB
+ $&gain_ripple >> lna_core_06V_cgcs_report.txt
echo S12_MIN_DB $&s12min AT_HZ $&s12min_f S12_MAX_DB $&s12max AT_HZ $&s12max_f >>
+ lna_core_06V_cgcs_report.txt
echo S22_MIN_DB $&s22min AT_HZ $&s22min_f S22_MAX_DB $&s22max AT_HZ $&s22max_f >>
+ lna_core_06V_cgcs_report.txt
echo NF_MIN_DB $&nfbandmin AT_HZ $&nfmin_f NF_MAX_DB $&nfbandmax AT_HZ $&nfmax_f >>
+ lna_core_06V_cgcs_report.txt
echo NFMIN_PARAMETER_MIN_DB $&nfminbandmin AT_HZ $&nfminpar_min_f NFMIN_PARAMETER_MAX_DB
+ $&nfminbandmax AT_HZ $&nfminpar_max_f >> lna_core_06V_cgcs_report.txt
echo MU_MIN $&mumin AT_HZ $&mumin_f MUP_MIN $&mupmin AT_HZ $&mupmin_f >>
+ lna_core_06V_cgcs_report.txt
echo K_MIN $&kmin AT_HZ $&kmin_f DELTA_MAX $&dmax AT_HZ $&dmax_f >> lna_core_06V_cgcs_report.txt

echo ============================================================ >> lna_core_06V_cgcs_report.txt
echo BROADBAND_GAIN_CHECK_1MHZ_TO_7GHZ >> lna_core_06V_cgcs_report.txt
echo GAIN_AT_2P4_DB $&s21c >> lna_core_06V_cgcs_report.txt
echo BROADBAND_PEAK_HZ $&peakfreq PEAK_GAIN_DB $&gainmax >> lna_core_06V_cgcs_report.txt

echo ============================================================ >> lna_core_06V_cgcs_report.txt
echo TARGET_CENTERED_S21_GE_10DB_BAND >> lna_core_06V_cgcs_report.txt
if s21c >= 10.0
let bwlo=icenter
let bwhi=icenter
let search=1
while search = 1
if bwlo > 0
if s21db[bwlo-1] >= 10.0
let bwlo=bwlo-1
else
let search=0
end
else
let search=0
end
end
let search=1
while search = 1
if bwhi < npts-1
if s21db[bwhi+1] >= 10.0
let bwhi=bwhi+1
else
let search=0
end
else
let search=0
end
end
let bwflo=frequency[bwlo]
let bwfhi=frequency[bwhi]
let bwval=bwfhi-bwflo
let bwcenter=0.5*(bwfhi+bwflo)
let bwfbw=100*bwval/(bwcenter+1e-30)
echo LOWER_HZ $&bwflo UPPER_HZ $&bwfhi BANDWIDTH_HZ $&bwval BAND_CENTER_HZ $&bwcenter
+ FRACTIONAL_BW_PERCENT $&bwfbw >> lna_core_06V_cgcs_report.txt
else
echo NO_VALID_TARGET_CENTERED_BAND S21_AT_2P4_DB $&s21c >> lna_core_06V_cgcs_report.txt
end

echo ============================================================ >> lna_core_06V_cgcs_report.txt
echo GLOBAL_CONTIGUOUS_S21_GE_10DB_BAND_AROUND_PEAK >> lna_core_06V_cgcs_report.txt
if gainmax >= 10.0
let bwlo=imax
let bwhi=imax
let search=1
while search = 1
if bwlo > 0
if s21db[bwlo-1] >= 10.0
let bwlo=bwlo-1
else
let search=0
end
else
let search=0
end
end
let search=1
while search = 1
if bwhi < npts-1
if s21db[bwhi+1] >= 10.0
let bwhi=bwhi+1
else
let search=0
end
else
let search=0
end
end
let bwflo=frequency[bwlo]
let bwfhi=frequency[bwhi]
let bwval=bwfhi-bwflo
let bwcenter=0.5*(bwfhi+bwflo)
let bwfbw=100*bwval/(bwcenter+1e-30)
echo LOWER_HZ $&bwflo UPPER_HZ $&bwfhi BANDWIDTH_HZ $&bwval BAND_CENTER_HZ $&bwcenter
+ FRACTIONAL_BW_PERCENT $&bwfbw >> lna_core_06V_cgcs_report.txt
else
echo NO_S21_ABOVE_10DB_FROM_1MHZ_TO_7GHZ PEAK_GAIN_DB $&gainmax PEAK_FREQUENCY_HZ $&peakfreq >>
+ lna_core_06V_cgcs_report.txt
end

wrdata lna_core_06V_cgcs_target_band.dat frequency s_1_1 s_2_1 s_1_2 s_2_2 s11db s21db s12db s22db
+ nfdb nfmin_db kval mu mup delta_mag zin_re zin_im zout_re zout_im
wrdata lna_core_06V_cgcs_broadband.dat frequency s11db s21db s12db s22db nfdb nfmin_db kval mu mup
+ delta_mag zin_re zin_im zout_re zout_im

* =============================================================================
* NOISE-CANCELLATION A/B PROOF
*
* ON baseline:
*   CNC = optimized value (8.2 pF).
*
* OFF baseline:
*   CNC is opened to 1e-18 F using alterparam.
*   XM7/XM9 remain biased and connected to vx, so their DC current,
*   output loading and intrinsic noise remain present. Only the sensed
*   RF path from node s to g_csc is removed. This is a conservative
*   demonstration of whether the sensing/cancellation action reduces NF.
*
* Positive NF_IMPROVEMENT_DB = NF_OFF - NF_ON means cancellation helps.
* =============================================================================

* Preserve the cancellation-ON plot generated above.
set nc_on_plot=$rfplot

* Open only the noise-sensing capacitor.
alterparam CNC_VAL = 1e-18
reset

sp lin 7000 1Meg 7Gig 1
set nc_off_plot=$curplot

let fghz_nc=frequency/1e9

* Copy ON data into this plot so ON and OFF vectors share one scale.
let nf_nc_on={$nc_on_plot}.nfdb
let s21_nc_on={$nc_on_plot}.s21db
let s11_nc_on={$nc_on_plot}.s11db
let s22_nc_on={$nc_on_plot}.s22db

* OFF data with the cancellation sensing path opened.
let nf_nc_off=real(NF)
let s21_nc_off=db(s_2_1)
let s11_nc_off=db(s_1_1)
let s22_nc_off=db(s_2_2)

* Main proof vector. Positive values mean lower NF with cancellation ON.
let nf_improvement_db=nf_nc_off-nf_nc_on
let gain_change_on_minus_off_db=s21_nc_on-s21_nc_off

let nc_npts=length(frequency)

* Locate 2.3, 2.4 and 2.5 GHz in the OFF dataset.
let nc_ilo=0
let nc_icenter=0
let nc_ihi=0
let nc_errlo=abs(frequency[0]-2.3e9)
let nc_errcenter=abs(frequency[0]-2.4e9)
let nc_errhi=abs(frequency[0]-2.5e9)
let nc_ii=1
while nc_ii < nc_npts
  let nc_newerr=abs(frequency[nc_ii]-2.3e9)
  if nc_newerr < nc_errlo
    let nc_errlo=nc_newerr
    let nc_ilo=nc_ii
  end

  let nc_newerr=abs(frequency[nc_ii]-2.4e9)
  if nc_newerr < nc_errcenter
    let nc_errcenter=nc_newerr
    let nc_icenter=nc_ii
  end

  let nc_newerr=abs(frequency[nc_ii]-2.5e9)
  if nc_newerr < nc_errhi
    let nc_errhi=nc_newerr
    let nc_ihi=nc_ii
  end

  let nc_ii=nc_ii+1
end

* Center-frequency results.
let nc_freq_center=frequency[nc_icenter]
let nc_nf_on_c=nf_nc_on[nc_icenter]
let nc_nf_off_c=nf_nc_off[nc_icenter]
let nc_imp_c=nf_improvement_db[nc_icenter]

let nc_s21_on_c=s21_nc_on[nc_icenter]
let nc_s21_off_c=s21_nc_off[nc_icenter]
let nc_gain_delta_c=gain_change_on_minus_off_db[nc_icenter]

let nc_s11_on_c=s11_nc_on[nc_icenter]
let nc_s11_off_c=s11_nc_off[nc_icenter]
let nc_s22_on_c=s22_nc_on[nc_icenter]
let nc_s22_off_c=s22_nc_off[nc_icenter]

* Improvement extrema over 2.3-2.5 GHz.
let nc_imp_min=nf_improvement_db[nc_ilo]
let nc_imp_max=nf_improvement_db[nc_ilo]
let nc_imp_min_i=nc_ilo
let nc_imp_max_i=nc_ilo

let nc_ii=nc_ilo
while nc_ii <= nc_ihi
  if nf_improvement_db[nc_ii] < nc_imp_min
    let nc_imp_min=nf_improvement_db[nc_ii]
    let nc_imp_min_i=nc_ii
  end
  if nf_improvement_db[nc_ii] > nc_imp_max
    let nc_imp_max=nf_improvement_db[nc_ii]
    let nc_imp_max_i=nc_ii
  end
  let nc_ii=nc_ii+1
end

let nc_imp_min_f=frequency[nc_imp_min_i]
let nc_imp_max_f=frequency[nc_imp_max_i]

* User-selectable threshold for a practically meaningful center improvement.
let nc_practical_threshold_db=0.20

echo ============================================================ >> lna_core_06V_cgcs_report.txt
echo NOISE_CANCELLATION_AB_PROOF >> lna_core_06V_cgcs_report.txt
echo METHOD ON_CNC_8P2PF OFF_CNC_1E_MINUS18F_XM7_XM9_STILL_BIASED_AND_LOADING_RETAINED >>
+ lna_core_06V_cgcs_report.txt
echo ACTUAL_CENTER_SAMPLE_HZ $&nc_freq_center >> lna_core_06V_cgcs_report.txt
echo NF_ON_DB $&nc_nf_on_c NF_OFF_DB $&nc_nf_off_c NF_IMPROVEMENT_DB $&nc_imp_c >>
+ lna_core_06V_cgcs_report.txt
echo S21_ON_DB $&nc_s21_on_c S21_OFF_DB $&nc_s21_off_c S21_ON_MINUS_OFF_DB $&nc_gain_delta_c >>
+ lna_core_06V_cgcs_report.txt
echo S11_ON_DB $&nc_s11_on_c S11_OFF_DB $&nc_s11_off_c >> lna_core_06V_cgcs_report.txt
echo S22_ON_DB $&nc_s22_on_c S22_OFF_DB $&nc_s22_off_c >> lna_core_06V_cgcs_report.txt
echo NF_IMPROVEMENT_MIN_DB_2P3_TO_2P5 $&nc_imp_min AT_HZ $&nc_imp_min_f >>
+ lna_core_06V_cgcs_report.txt
echo NF_IMPROVEMENT_MAX_DB_2P3_TO_2P5 $&nc_imp_max AT_HZ $&nc_imp_max_f >>
+ lna_core_06V_cgcs_report.txt
echo PRACTICAL_CENTER_THRESHOLD_DB $&nc_practical_threshold_db >> lna_core_06V_cgcs_report.txt

if nc_imp_c > 0
  echo CENTER_DIRECTIONAL_TEST PASS_CANCELLATION_LOWERS_NF >> lna_core_06V_cgcs_report.txt
else
  echo CENTER_DIRECTIONAL_TEST FAIL_CANCELLATION_DOES_NOT_LOWER_NF >> lna_core_06V_cgcs_report.txt
end

if nc_imp_min > 0
  echo FULL_TARGET_BAND_TEST PASS_CANCELLATION_LOWERS_NF_ACROSS_2P3_TO_2P5_GHZ >>
+ lna_core_06V_cgcs_report.txt
else
  echo FULL_TARGET_BAND_TEST FAIL_NF_IMPROVEMENT_NOT_POSITIVE_ACROSS_ENTIRE_TARGET_BAND >>
+ lna_core_06V_cgcs_report.txt
end

if nc_imp_c >= nc_practical_threshold_db
  echo PRACTICAL_CENTER_TEST PASS_IMPROVEMENT_AT_LEAST_0P20_DB >> lna_core_06V_cgcs_report.txt
else
  echo PRACTICAL_CENTER_TEST FAIL_IMPROVEMENT_BELOW_0P20_DB >> lna_core_06V_cgcs_report.txt
end

wrdata lna_core_06V_cgcs_noise_cancellation.dat nf_nc_on nf_nc_off nf_improvement_db s21_nc_on
+ s21_nc_off s11_nc_on s11_nc_off s22_nc_on s22_nc_off

* Restore the optimized cancellation capacitor before subsequent analyses.
alterparam CNC_VAL = 8.2p
reset

* =============================================================================
* WIDEBAND STABILITY 10 MHZ TO 30 GHZ
* =============================================================================

sp dec 101 10Meg 30G 1
set stabilityplot=$curplot

let wbdelta=s_1_1*s_2_2-s_1_2*s_2_1
let wbmd=mag(wbdelta)
let wba11=mag(s_1_1)
let wba12=mag(s_1_2)
let wba21=mag(s_2_1)
let wba22=mag(s_2_2)
let wbmu=(1-wba11*wba11)/(mag(s_2_2-wbdelta*conj(s_1_1))+mag(s_1_2*s_2_1))
let wbmup=(1-wba22*wba22)/(mag(s_1_1-wbdelta*conj(s_2_2))+mag(s_1_2*s_2_1))
let wbk=(1-wba11*wba11-wba22*wba22+wbmd*wbmd)/(2*wba12*wba21)

let wbkmin=minimum(wbk)
let wbmumin=minimum(wbmu)
let wbmupmin=minimum(wbmup)
let wbdmax=maximum(wbmd)

set final_wbkmin=$&wbkmin
set final_wbmumin=$&wbmumin
set final_wbmupmin=$&wbmupmin
set final_wbdmax=$&wbdmax

echo ============================================================ >> lna_core_06V_cgcs_report.txt
echo WIDEBAND_STABILITY_10MHZ_TO_30GHZ >> lna_core_06V_cgcs_report.txt
echo K_MIN $final_wbkmin MU_MIN $final_wbmumin MUP_MIN $final_wbmupmin DELTA_MAX $final_wbdmax >>
+ lna_core_06V_cgcs_report.txt

wrdata lna_core_06V_cgcs_stability.dat frequency wbk wbmu wbmup wbmd

let wbfghz=frequency/1e9

echo ============================================================ >> lna_core_06V_cgcs_report.txt
echo OUTPUT_FILES >> lna_core_06V_cgcs_report.txt
echo REPORT lna_core_06V_cgcs_report.txt >> lna_core_06V_cgcs_report.txt
echo TARGET_DATA lna_core_06V_cgcs_target_band.dat >> lna_core_06V_cgcs_report.txt
echo BROADBAND_DATA lna_core_06V_cgcs_broadband.dat >> lna_core_06V_cgcs_report.txt
echo STABILITY_DATA lna_core_06V_cgcs_stability.dat >> lna_core_06V_cgcs_report.txt
echo NOISE_CANCELLATION_DATA lna_core_06V_cgcs_noise_cancellation.dat >>
+ lna_core_06V_cgcs_report.txt
echo PLOTS S_PARAMETERS NF_NFMIN NOISE_CANCELLATION_ON_OFF NF_IMPROVEMENT S21_ON_OFF >>
+ lna_core_06V_cgcs_report.txt
echo ============================================================ >> lna_core_06V_cgcs_report.txt



* =============================================================================
* VISIBLE PLOTS
* Plot commands are intentionally placed at the very end.
* Neither rfplot nor stabilityplot is destroyed or reset afterward.
* =============================================================================

setplot $rfplot
setscale fghz

* Target band 2.3 GHz to 2.5 GHz
plot s11db xlimit 2.3 2.5
plot s21db xlimit 2.3 2.5
plot s12db xlimit 2.3 2.5
plot s22db xlimit 2.3 2.5
plot nfdb nfmin_db xlimit 2.3 2.5
* plot mu mup xlimit 2.3 2.5
* plot kval xlimit 2.3 2.5
* plot delta_mag xlimit 2.3 2.5
* plot zin_re zin_im xlimit 2.3 2.5
* plot zout_re zout_im xlimit 2.3 2.5

* Broadband 1 MHz to 7 GHz
plot s11db xlimit 0 7
plot s21db xlimit 0 7
plot s12db xlimit 0 7
plot s22db xlimit 0 7
plot nfdb nfmin_db xlimit 0 7
* plot mu mup xlimit 0 7
* plot kval xlimit 0 7
* plot delta_mag xlimit 0 7
* plot zin_re zin_im xlimit 0 7
* plot zout_re zout_im xlimit 0 7

* Noise-cancellation proof plots
setplot $nc_off_plot
setscale fghz_nc
set xbrushwidth=2

* Plot 1: direct NF comparison; ON must lie below OFF.
plot nf_nc_on nf_nc_off xlimit 2.3 2.5 xlabel 'Frequency (GHz)' ylabel 'Noise figure (dB)'

* Plot 2: positive improvement proves cancellation benefit.
plot nf_improvement_db xlimit 2.3 2.5 xlabel 'Frequency (GHz)' ylabel 'NF OFF - NF ON (dB)'

* Plot 3: signal-gain sanity check for the same A/B experiment.
plot s21_nc_on s21_nc_off xlimit 2.3 2.5 xlabel 'Frequency (GHz)' ylabel 'S21 (dB)'

* Wideband stability 10 MHz to 30 GHz
* setplot $stabilityplot
* setscale wbfghz
* plot wbmu wbmup
* plot wbk
* plot wbmd

.endc



**** end user architecture code
**.ends
.GLOBAL GND
.end
